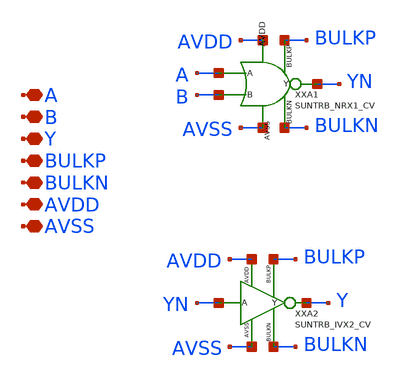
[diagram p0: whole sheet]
** sch_path: ip/sun_trb_sky130nm/design/SUN_TRB_SKY130NM/SUNTRB_ORX2_CV.sch
**.subckt SUNTRB_ORX2_CV A B Y BULKP BULKN AVDD AVSS
*.iopin A
*.iopin B
*.iopin Y
*.iopin BULKP
*.iopin BULKN
*.iopin AVDD
*.iopin AVSS
XXA2 YN Y BULKP BULKN AVDD AVSS SUNTRB_IVX2_CV xoffset=0 yoffset=0 angle=0
**.ends
.end
